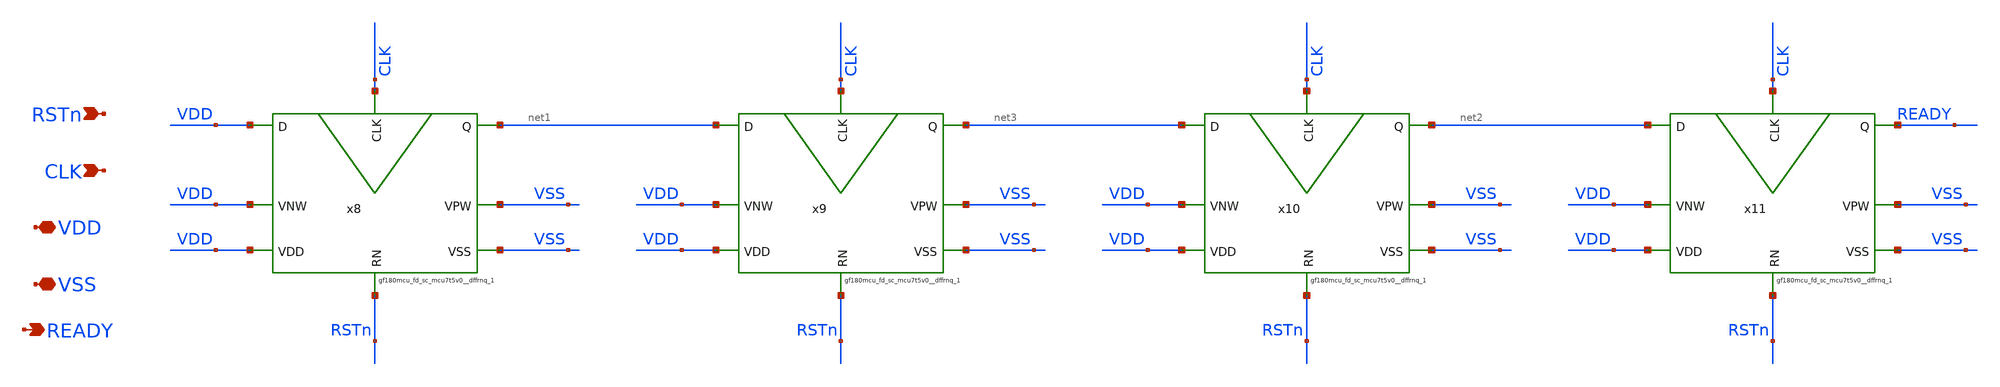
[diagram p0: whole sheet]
** sch_path: RDY/RDY.sch
**.subckt RDY RSTn CLK VDD VSS READY
*.ipin RSTn
*.ipin CLK
*.iopin VDD
*.iopin VSS
*.opin READY
x8 VDD RSTn CLK net1 VDD VDD VSS VSS gf180mcu_fd_sc_mcu7t5v0__dffrnq_1
x9 net1 RSTn CLK net3 VDD VDD VSS VSS gf180mcu_fd_sc_mcu7t5v0__dffrnq_1
x10 net3 RSTn CLK net2 VDD VDD VSS VSS gf180mcu_fd_sc_mcu7t5v0__dffrnq_1
x11 net2 RSTn CLK READY VDD VDD VSS VSS gf180mcu_fd_sc_mcu7t5v0__dffrnq_1
**.ends
.end
